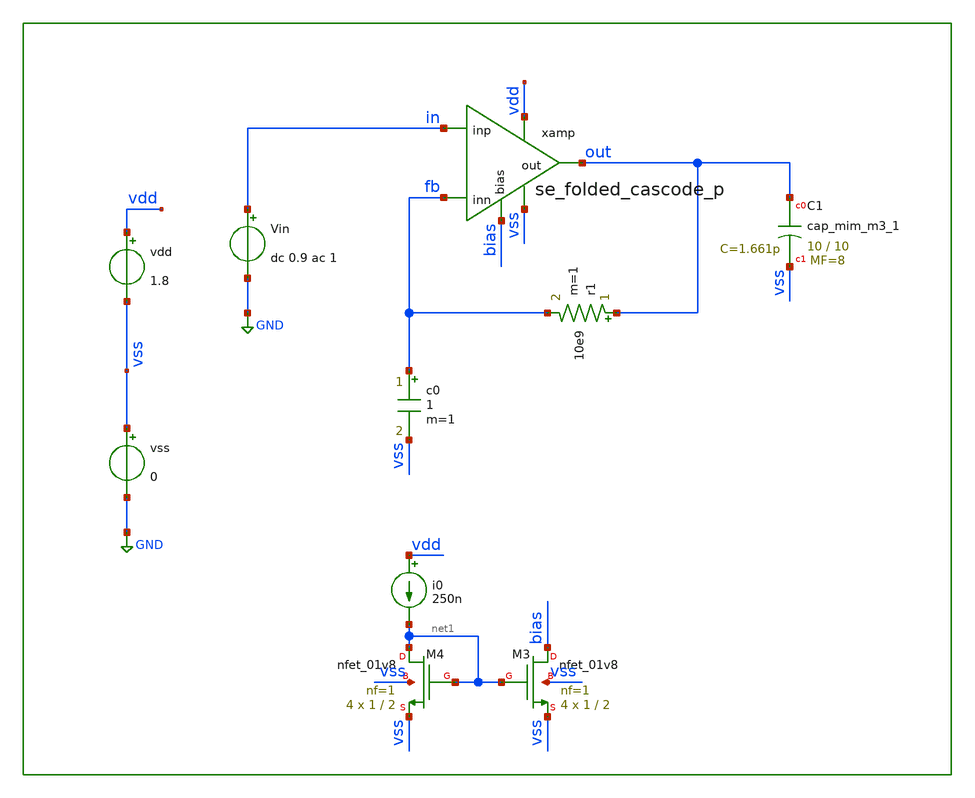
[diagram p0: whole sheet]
** sch_path: xschem/tb/opamp/ac_se_folded_ota_p.sch
**.subckt ac_se_folded_ota_p
vss vss GND 0
vdd vdd vss 1.8
Vin in GND dc 0.9 ac 1
c0 fb vss 1 m=1
r1 out fb 10e9 m=1
i0 vdd net1 250n
XM3 bias net1 vss vss sky130_fd_pr__nfet_01v8 L=2 W=1 nf=1 ad='int((nf+1)/2) * W/nf * 0.29' as='int((nf+2)/2) * W/nf * 0.29'
+ pd='2*int((nf+1)/2) * (W/nf + 0.29)' ps='2*int((nf+2)/2) * (W/nf + 0.29)' nrd='0.29 / W' nrs='0.29 / W'
+ sa=0 sb=0 sd=0 mult=4 m=4
XM4 net1 net1 vss vss sky130_fd_pr__nfet_01v8 L=2 W=1 nf=1 ad='int((nf+1)/2) * W/nf * 0.29' as='int((nf+2)/2) * W/nf * 0.29'
+ pd='2*int((nf+1)/2) * (W/nf + 0.29)' ps='2*int((nf+2)/2) * (W/nf + 0.29)' nrd='0.29 / W' nrs='0.29 / W'
+ sa=0 sb=0 sd=0 mult=4 m=4
xamp vdd out in fb vss bias se_folded_cascode_p
XC1 out vss sky130_fd_pr__cap_mim_m3_1 W=10 L=10 MF=8 m=8
**** begin user architecture code

* ac se_folded_cascode_p

.param MC_SWITCH=0
*.temp 85

*.include \$::DESIGN_PATH\/opamp/se_folded_cascode_p.pex.spice"

.control
save all
ac dec 10 1 100e6
let phase=180/3.14*cph(out)
let phase=180 + 180/3.14*cph(out)
meas ac ugbw when vdb(out)=0
meas ac pm find phase when vdb(out)=0
meas ac gain find vdb(out) at=1

*let mc_runs = 500
*let run = 1
*dowhile run <= mc_runs
*    save all
*    ac dec 10 1 100e6
*    let phase=180/3.14*cph(out)
*    let phase=180 + 180/3.14*cph(out)
*    meas ac ugbw when vdb(out)=0
*    meas ac pm find phase when vdb(out)=0
*    meas ac gain find vdb(out) at=100
*    print gain >> result_gain.txt
*    print pm >> result_pm.txt
*    print ugbw >> result_ugbw.txt
*    reset
*    let run = run + 1
*end


.endc


 .include $::SKYWATER_STDCELLS/cells/inv/sky130_fd_sc_hd__inv_1.spice

* FET CORNERS
.include $::SKYWATER_MODELS/corners/tt.spice
*.include $::SKYWATER_MODELS/corners/ff.spice
*.include $::SKYWATER_MODELS/corners/ss.spice
*.include $::SKYWATER_MODELS/corners/sf.spice
*.include $::SKYWATER_MODELS/corners/fs.spice

* TT + R + C
*.include $::SKYWATER_MODELS/corners/tt_rmax_cmax.spice
*.include $::SKYWATER_MODELS/corners/tt_rmin_cmin.spice
*.include $::SKYWATER_MODELS/corners/tt_rmax_cmin.spice
*.include $::SKYWATER_MODELS/corners/tt_rmin_cmax.spice

* FF + R + C
*.include $::SKYWATER_MODELS/corners/ff_rmax_cmax.spice
*.include $::SKYWATER_MODELS/corners/ff_rmin_cmin.spice
*.include $::SKYWATER_MODELS/corners/ff_rmax_cmin.spice
*.include $::SKYWATER_MODELS/corners/ff_rmin_cmax.spice


* SS + R + C
*.include $::SKYWATER_MODELS/corners/ss_rmax_cmax.spice
*.include $::SKYWATER_MODELS/corners/ss_rmin_cmin.spice
*.include $::SKYWATER_MODELS/corners/ss_rmax_cmin.spice
*.include $::SKYWATER_MODELS/corners/ss_rmin_cmax.spice

* SF + R + C
*.include $::SKYWATER_MODELS/corners/sf_rmax_cmax.spice
*.include $::SKYWATER_MODELS/corners/sf_rmin_cmin.spice
*.include $::SKYWATER_MODELS/corners/sf_rmax_cmin.spice
*.include $::SKYWATER_MODELS/corners/sf_rmin_cmax.spice

* FS + R + C
*.include $::SKYWATER_MODELS/corners/fs_rmax_cmax.spice
*.include $::SKYWATER_MODELS/corners/fs_rmin_cmin.spice
*.include $::SKYWATER_MODELS/corners/fs_rmax_cmin.spice
*.include $::SKYWATER_MODELS/corners/fs_rmin_cmax.spice

**** end user architecture code
**.ends

* expanding   symbol:  opamp/se_folded_cascode_p.sym # of pins=6
** sym_path: xschem/opamp/se_folded_cascode_p.sym
** sch_path: xschem/opamp/se_folded_cascode_p.sch
.subckt se_folded_cascode_p vdd out inp inn vss bias
*.ipin inn
*.ipin inp
*.opin out
*.iopin bias
*.iopin vdd
*.iopin vss
XM3 out1p inn diff vdd sky130_fd_pr__pfet_01v8_lvt L=1 W=4 nf=1 ad='int((nf+1)/2) * W/nf * 0.29' as='int((nf+2)/2) * W/nf * 0.29'
+ pd='2*int((nf+1)/2) * (W/nf + 0.29)' ps='2*int((nf+2)/2) * (W/nf + 0.29)' nrd='0.29 / W' nrs='0.29 / W'
+ sa=0 sb=0 sd=0 mult=8 m=8
XM2 out1n inp diff vdd sky130_fd_pr__pfet_01v8_lvt L=1 W=4 nf=1 ad='int((nf+1)/2) * W/nf * 0.29' as='int((nf+2)/2) * W/nf * 0.29'
+ pd='2*int((nf+1)/2) * (W/nf + 0.29)' ps='2*int((nf+2)/2) * (W/nf + 0.29)' nrd='0.29 / W' nrs='0.29 / W'
+ sa=0 sb=0 sd=0 mult=8 m=8
XM1 diff vbp1 vdd vdd sky130_fd_pr__pfet_01v8_lvt L=1 W=1 nf=1 ad='int((nf+1)/2) * W/nf * 0.29' as='int((nf+2)/2) * W/nf * 0.29'
+ pd='2*int((nf+1)/2) * (W/nf + 0.29)' ps='2*int((nf+2)/2) * (W/nf + 0.29)' nrd='0.29 / W' nrs='0.29 / W'
+ sa=0 sb=0 sd=0 mult=14 m=14
XM4 out1n vbn1 vss vss sky130_fd_pr__nfet_01v8_lvt L=1 W=1 nf=1 ad='int((nf+1)/2) * W/nf * 0.29' as='int((nf+2)/2) * W/nf * 0.29'
+ pd='2*int((nf+1)/2) * (W/nf + 0.29)' ps='2*int((nf+2)/2) * (W/nf + 0.29)' nrd='0.29 / W' nrs='0.29 / W'
+ sa=0 sb=0 sd=0 mult=16 m=16
XM5 out1p vbn1 vss vss sky130_fd_pr__nfet_01v8_lvt L=1 W=1 nf=1 ad='int((nf+1)/2) * W/nf * 0.29' as='int((nf+2)/2) * W/nf * 0.29'
+ pd='2*int((nf+1)/2) * (W/nf + 0.29)' ps='2*int((nf+2)/2) * (W/nf + 0.29)' nrd='0.29 / W' nrs='0.29 / W'
+ sa=0 sb=0 sd=0 mult=16 m=16
XM6 mirr vbn2 out1n vss sky130_fd_pr__nfet_01v8_lvt L=4 W=1 nf=1 ad='int((nf+1)/2) * W/nf * 0.29' as='int((nf+2)/2) * W/nf * 0.29'
+ pd='2*int((nf+1)/2) * (W/nf + 0.29)' ps='2*int((nf+2)/2) * (W/nf + 0.29)' nrd='0.29 / W' nrs='0.29 / W'
+ sa=0 sb=0 sd=0 mult=8 m=8
XM7 out vbn2 out1p vss sky130_fd_pr__nfet_01v8_lvt L=4 W=1 nf=1 ad='int((nf+1)/2) * W/nf * 0.29' as='int((nf+2)/2) * W/nf * 0.29'
+ pd='2*int((nf+1)/2) * (W/nf + 0.29)' ps='2*int((nf+2)/2) * (W/nf + 0.29)' nrd='0.29 / W' nrs='0.29 / W'
+ sa=0 sb=0 sd=0 mult=8 m=8
XM8 mirr bias nd10 vdd sky130_fd_pr__pfet_01v8_lvt L=4 W=2 nf=1 ad='int((nf+1)/2) * W/nf * 0.29' as='int((nf+2)/2) * W/nf * 0.29'
+ pd='2*int((nf+1)/2) * (W/nf + 0.29)' ps='2*int((nf+2)/2) * (W/nf + 0.29)' nrd='0.29 / W' nrs='0.29 / W'
+ sa=0 sb=0 sd=0 mult=8 m=8
XM9 out bias nd11 vdd sky130_fd_pr__pfet_01v8_lvt L=4 W=2 nf=1 ad='int((nf+1)/2) * W/nf * 0.29' as='int((nf+2)/2) * W/nf * 0.29'
+ pd='2*int((nf+1)/2) * (W/nf + 0.29)' ps='2*int((nf+2)/2) * (W/nf + 0.29)' nrd='0.29 / W' nrs='0.29 / W'
+ sa=0 sb=0 sd=0 mult=8 m=8
XM10 nd10 mirr vdd vdd sky130_fd_pr__pfet_01v8_lvt L=4 W=2 nf=1 ad='int((nf+1)/2) * W/nf * 0.29' as='int((nf+2)/2) * W/nf * 0.29'
+ pd='2*int((nf+1)/2) * (W/nf + 0.29)' ps='2*int((nf+2)/2) * (W/nf + 0.29)' nrd='0.29 / W' nrs='0.29 / W'
+ sa=0 sb=0 sd=0 mult=8 m=8
XM11 nd11 mirr vdd vdd sky130_fd_pr__pfet_01v8_lvt L=4 W=2 nf=1 ad='int((nf+1)/2) * W/nf * 0.29' as='int((nf+2)/2) * W/nf * 0.29'
+ pd='2*int((nf+1)/2) * (W/nf + 0.29)' ps='2*int((nf+2)/2) * (W/nf + 0.29)' nrd='0.29 / W' nrs='0.29 / W'
+ sa=0 sb=0 sd=0 mult=8 m=8
XMB1 bias bias vbp1 vdd sky130_fd_pr__pfet_01v8_lvt L=4 W=2 nf=1 ad='int((nf+1)/2) * W/nf * 0.29' as='int((nf+2)/2) * W/nf * 0.29'
+ pd='2*int((nf+1)/2) * (W/nf + 0.29)' ps='2*int((nf+2)/2) * (W/nf + 0.29)' nrd='0.29 / W' nrs='0.29 / W'
+ sa=0 sb=0 sd=0 mult=4 m=4
XMB2 vbp1 vbp1 vdd vdd sky130_fd_pr__pfet_01v8_lvt L=1 W=1 nf=1 ad='int((nf+1)/2) * W/nf * 0.29' as='int((nf+2)/2) * W/nf * 0.29'
+ pd='2*int((nf+1)/2) * (W/nf + 0.29)' ps='2*int((nf+2)/2) * (W/nf + 0.29)' nrd='0.29 / W' nrs='0.29 / W'
+ sa=0 sb=0 sd=0 mult=4 m=4
XMB3 vbn2 vbp1 vdd vdd sky130_fd_pr__pfet_01v8_lvt L=1 W=1 nf=1 ad='int((nf+1)/2) * W/nf * 0.29' as='int((nf+2)/2) * W/nf * 0.29'
+ pd='2*int((nf+1)/2) * (W/nf + 0.29)' ps='2*int((nf+2)/2) * (W/nf + 0.29)' nrd='0.29 / W' nrs='0.29 / W'
+ sa=0 sb=0 sd=0 mult=4 m=4
XMB4 vbn2 vbn2 vbn1 vss sky130_fd_pr__nfet_01v8_lvt L=4 W=1 nf=1 ad='int((nf+1)/2) * W/nf * 0.29' as='int((nf+2)/2) * W/nf * 0.29'
+ pd='2*int((nf+1)/2) * (W/nf + 0.29)' ps='2*int((nf+2)/2) * (W/nf + 0.29)' nrd='0.29 / W' nrs='0.29 / W'
+ sa=0 sb=0 sd=0 mult=4 m=4
XMB5 vbn1 vbn1 vss vss sky130_fd_pr__nfet_01v8_lvt L=1 W=1 nf=1 ad='int((nf+1)/2) * W/nf * 0.29' as='int((nf+2)/2) * W/nf * 0.29'
+ pd='2*int((nf+1)/2) * (W/nf + 0.29)' ps='2*int((nf+2)/2) * (W/nf + 0.29)' nrd='0.29 / W' nrs='0.29 / W'
+ sa=0 sb=0 sd=0 mult=4 m=4
XMDUM1[43] vdd vdd vdd vdd sky130_fd_pr__pfet_01v8_lvt L=4 W=2 nf=1 ad='int((nf+1)/2) * W/nf * 0.29'
+ as='int((nf+2)/2) * W/nf * 0.29' pd='2*int((nf+1)/2) * (W/nf + 0.29)' ps='2*int((nf+2)/2) * (W/nf + 0.29)'
+ nrd='0.29 / W' nrs='0.29 / W' sa=0 sb=0 sd=0 mult=1 m=1
XMDUM1[42] vdd vdd vdd vdd sky130_fd_pr__pfet_01v8_lvt L=4 W=2 nf=1 ad='int((nf+1)/2) * W/nf * 0.29'
+ as='int((nf+2)/2) * W/nf * 0.29' pd='2*int((nf+1)/2) * (W/nf + 0.29)' ps='2*int((nf+2)/2) * (W/nf + 0.29)'
+ nrd='0.29 / W' nrs='0.29 / W' sa=0 sb=0 sd=0 mult=1 m=1
XMDUM1[41] vdd vdd vdd vdd sky130_fd_pr__pfet_01v8_lvt L=4 W=2 nf=1 ad='int((nf+1)/2) * W/nf * 0.29'
+ as='int((nf+2)/2) * W/nf * 0.29' pd='2*int((nf+1)/2) * (W/nf + 0.29)' ps='2*int((nf+2)/2) * (W/nf + 0.29)'
+ nrd='0.29 / W' nrs='0.29 / W' sa=0 sb=0 sd=0 mult=1 m=1
XMDUM1[40] vdd vdd vdd vdd sky130_fd_pr__pfet_01v8_lvt L=4 W=2 nf=1 ad='int((nf+1)/2) * W/nf * 0.29'
+ as='int((nf+2)/2) * W/nf * 0.29' pd='2*int((nf+1)/2) * (W/nf + 0.29)' ps='2*int((nf+2)/2) * (W/nf + 0.29)'
+ nrd='0.29 / W' nrs='0.29 / W' sa=0 sb=0 sd=0 mult=1 m=1
XMDUM1[39] vdd vdd vdd vdd sky130_fd_pr__pfet_01v8_lvt L=4 W=2 nf=1 ad='int((nf+1)/2) * W/nf * 0.29'
+ as='int((nf+2)/2) * W/nf * 0.29' pd='2*int((nf+1)/2) * (W/nf + 0.29)' ps='2*int((nf+2)/2) * (W/nf + 0.29)'
+ nrd='0.29 / W' nrs='0.29 / W' sa=0 sb=0 sd=0 mult=1 m=1
XMDUM1[38] vdd vdd vdd vdd sky130_fd_pr__pfet_01v8_lvt L=4 W=2 nf=1 ad='int((nf+1)/2) * W/nf * 0.29'
+ as='int((nf+2)/2) * W/nf * 0.29' pd='2*int((nf+1)/2) * (W/nf + 0.29)' ps='2*int((nf+2)/2) * (W/nf + 0.29)'
+ nrd='0.29 / W' nrs='0.29 / W' sa=0 sb=0 sd=0 mult=1 m=1
XMDUM1[37] vdd vdd vdd vdd sky130_fd_pr__pfet_01v8_lvt L=4 W=2 nf=1 ad='int((nf+1)/2) * W/nf * 0.29'
+ as='int((nf+2)/2) * W/nf * 0.29' pd='2*int((nf+1)/2) * (W/nf + 0.29)' ps='2*int((nf+2)/2) * (W/nf + 0.29)'
+ nrd='0.29 / W' nrs='0.29 / W' sa=0 sb=0 sd=0 mult=1 m=1
XMDUM1[36] vdd vdd vdd vdd sky130_fd_pr__pfet_01v8_lvt L=4 W=2 nf=1 ad='int((nf+1)/2) * W/nf * 0.29'
+ as='int((nf+2)/2) * W/nf * 0.29' pd='2*int((nf+1)/2) * (W/nf + 0.29)' ps='2*int((nf+2)/2) * (W/nf + 0.29)'
+ nrd='0.29 / W' nrs='0.29 / W' sa=0 sb=0 sd=0 mult=1 m=1
XMDUM1[35] vdd vdd vdd vdd sky130_fd_pr__pfet_01v8_lvt L=4 W=2 nf=1 ad='int((nf+1)/2) * W/nf * 0.29'
+ as='int((nf+2)/2) * W/nf * 0.29' pd='2*int((nf+1)/2) * (W/nf + 0.29)' ps='2*int((nf+2)/2) * (W/nf + 0.29)'
+ nrd='0.29 / W' nrs='0.29 / W' sa=0 sb=0 sd=0 mult=1 m=1
XMDUM1[34] vdd vdd vdd vdd sky130_fd_pr__pfet_01v8_lvt L=4 W=2 nf=1 ad='int((nf+1)/2) * W/nf * 0.29'
+ as='int((nf+2)/2) * W/nf * 0.29' pd='2*int((nf+1)/2) * (W/nf + 0.29)' ps='2*int((nf+2)/2) * (W/nf + 0.29)'
+ nrd='0.29 / W' nrs='0.29 / W' sa=0 sb=0 sd=0 mult=1 m=1
XMDUM1[33] vdd vdd vdd vdd sky130_fd_pr__pfet_01v8_lvt L=4 W=2 nf=1 ad='int((nf+1)/2) * W/nf * 0.29'
+ as='int((nf+2)/2) * W/nf * 0.29' pd='2*int((nf+1)/2) * (W/nf + 0.29)' ps='2*int((nf+2)/2) * (W/nf + 0.29)'
+ nrd='0.29 / W' nrs='0.29 / W' sa=0 sb=0 sd=0 mult=1 m=1
XMDUM1[32] vdd vdd vdd vdd sky130_fd_pr__pfet_01v8_lvt L=4 W=2 nf=1 ad='int((nf+1)/2) * W/nf * 0.29'
+ as='int((nf+2)/2) * W/nf * 0.29' pd='2*int((nf+1)/2) * (W/nf + 0.29)' ps='2*int((nf+2)/2) * (W/nf + 0.29)'
+ nrd='0.29 / W' nrs='0.29 / W' sa=0 sb=0 sd=0 mult=1 m=1
XMDUM1[31] vdd vdd vdd vdd sky130_fd_pr__pfet_01v8_lvt L=4 W=2 nf=1 ad='int((nf+1)/2) * W/nf * 0.29'
+ as='int((nf+2)/2) * W/nf * 0.29' pd='2*int((nf+1)/2) * (W/nf + 0.29)' ps='2*int((nf+2)/2) * (W/nf + 0.29)'
+ nrd='0.29 / W' nrs='0.29 / W' sa=0 sb=0 sd=0 mult=1 m=1
XMDUM1[30] vdd vdd vdd vdd sky130_fd_pr__pfet_01v8_lvt L=4 W=2 nf=1 ad='int((nf+1)/2) * W/nf * 0.29'
+ as='int((nf+2)/2) * W/nf * 0.29' pd='2*int((nf+1)/2) * (W/nf + 0.29)' ps='2*int((nf+2)/2) * (W/nf + 0.29)'
+ nrd='0.29 / W' nrs='0.29 / W' sa=0 sb=0 sd=0 mult=1 m=1
XMDUM1[29] vdd vdd vdd vdd sky130_fd_pr__pfet_01v8_lvt L=4 W=2 nf=1 ad='int((nf+1)/2) * W/nf * 0.29'
+ as='int((nf+2)/2) * W/nf * 0.29' pd='2*int((nf+1)/2) * (W/nf + 0.29)' ps='2*int((nf+2)/2) * (W/nf + 0.29)'
+ nrd='0.29 / W' nrs='0.29 / W' sa=0 sb=0 sd=0 mult=1 m=1
XMDUM1[28] vdd vdd vdd vdd sky130_fd_pr__pfet_01v8_lvt L=4 W=2 nf=1 ad='int((nf+1)/2) * W/nf * 0.29'
+ as='int((nf+2)/2) * W/nf * 0.29' pd='2*int((nf+1)/2) * (W/nf + 0.29)' ps='2*int((nf+2)/2) * (W/nf + 0.29)'
+ nrd='0.29 / W' nrs='0.29 / W' sa=0 sb=0 sd=0 mult=1 m=1
XMDUM1[27] vdd vdd vdd vdd sky130_fd_pr__pfet_01v8_lvt L=4 W=2 nf=1 ad='int((nf+1)/2) * W/nf * 0.29'
+ as='int((nf+2)/2) * W/nf * 0.29' pd='2*int((nf+1)/2) * (W/nf + 0.29)' ps='2*int((nf+2)/2) * (W/nf + 0.29)'
+ nrd='0.29 / W' nrs='0.29 / W' sa=0 sb=0 sd=0 mult=1 m=1
XMDUM1[26] vdd vdd vdd vdd sky130_fd_pr__pfet_01v8_lvt L=4 W=2 nf=1 ad='int((nf+1)/2) * W/nf * 0.29'
+ as='int((nf+2)/2) * W/nf * 0.29' pd='2*int((nf+1)/2) * (W/nf + 0.29)' ps='2*int((nf+2)/2) * (W/nf + 0.29)'
+ nrd='0.29 / W' nrs='0.29 / W' sa=0 sb=0 sd=0 mult=1 m=1
XMDUM1[25] vdd vdd vdd vdd sky130_fd_pr__pfet_01v8_lvt L=4 W=2 nf=1 ad='int((nf+1)/2) * W/nf * 0.29'
+ as='int((nf+2)/2) * W/nf * 0.29' pd='2*int((nf+1)/2) * (W/nf + 0.29)' ps='2*int((nf+2)/2) * (W/nf + 0.29)'
+ nrd='0.29 / W' nrs='0.29 / W' sa=0 sb=0 sd=0 mult=1 m=1
XMDUM1[24] vdd vdd vdd vdd sky130_fd_pr__pfet_01v8_lvt L=4 W=2 nf=1 ad='int((nf+1)/2) * W/nf * 0.29'
+ as='int((nf+2)/2) * W/nf * 0.29' pd='2*int((nf+1)/2) * (W/nf + 0.29)' ps='2*int((nf+2)/2) * (W/nf + 0.29)'
+ nrd='0.29 / W' nrs='0.29 / W' sa=0 sb=0 sd=0 mult=1 m=1
XMDUM1[23] vdd vdd vdd vdd sky130_fd_pr__pfet_01v8_lvt L=4 W=2 nf=1 ad='int((nf+1)/2) * W/nf * 0.29'
+ as='int((nf+2)/2) * W/nf * 0.29' pd='2*int((nf+1)/2) * (W/nf + 0.29)' ps='2*int((nf+2)/2) * (W/nf + 0.29)'
+ nrd='0.29 / W' nrs='0.29 / W' sa=0 sb=0 sd=0 mult=1 m=1
XMDUM1[22] vdd vdd vdd vdd sky130_fd_pr__pfet_01v8_lvt L=4 W=2 nf=1 ad='int((nf+1)/2) * W/nf * 0.29'
+ as='int((nf+2)/2) * W/nf * 0.29' pd='2*int((nf+1)/2) * (W/nf + 0.29)' ps='2*int((nf+2)/2) * (W/nf + 0.29)'
+ nrd='0.29 / W' nrs='0.29 / W' sa=0 sb=0 sd=0 mult=1 m=1
XMDUM1[21] vdd vdd vdd vdd sky130_fd_pr__pfet_01v8_lvt L=4 W=2 nf=1 ad='int((nf+1)/2) * W/nf * 0.29'
+ as='int((nf+2)/2) * W/nf * 0.29' pd='2*int((nf+1)/2) * (W/nf + 0.29)' ps='2*int((nf+2)/2) * (W/nf + 0.29)'
+ nrd='0.29 / W' nrs='0.29 / W' sa=0 sb=0 sd=0 mult=1 m=1
XMDUM1[20] vdd vdd vdd vdd sky130_fd_pr__pfet_01v8_lvt L=4 W=2 nf=1 ad='int((nf+1)/2) * W/nf * 0.29'
+ as='int((nf+2)/2) * W/nf * 0.29' pd='2*int((nf+1)/2) * (W/nf + 0.29)' ps='2*int((nf+2)/2) * (W/nf + 0.29)'
+ nrd='0.29 / W' nrs='0.29 / W' sa=0 sb=0 sd=0 mult=1 m=1
XMDUM1[19] vdd vdd vdd vdd sky130_fd_pr__pfet_01v8_lvt L=4 W=2 nf=1 ad='int((nf+1)/2) * W/nf * 0.29'
+ as='int((nf+2)/2) * W/nf * 0.29' pd='2*int((nf+1)/2) * (W/nf + 0.29)' ps='2*int((nf+2)/2) * (W/nf + 0.29)'
+ nrd='0.29 / W' nrs='0.29 / W' sa=0 sb=0 sd=0 mult=1 m=1
XMDUM1[18] vdd vdd vdd vdd sky130_fd_pr__pfet_01v8_lvt L=4 W=2 nf=1 ad='int((nf+1)/2) * W/nf * 0.29'
+ as='int((nf+2)/2) * W/nf * 0.29' pd='2*int((nf+1)/2) * (W/nf + 0.29)' ps='2*int((nf+2)/2) * (W/nf + 0.29)'
+ nrd='0.29 / W' nrs='0.29 / W' sa=0 sb=0 sd=0 mult=1 m=1
XMDUM1[17] vdd vdd vdd vdd sky130_fd_pr__pfet_01v8_lvt L=4 W=2 nf=1 ad='int((nf+1)/2) * W/nf * 0.29'
+ as='int((nf+2)/2) * W/nf * 0.29' pd='2*int((nf+1)/2) * (W/nf + 0.29)' ps='2*int((nf+2)/2) * (W/nf + 0.29)'
+ nrd='0.29 / W' nrs='0.29 / W' sa=0 sb=0 sd=0 mult=1 m=1
XMDUM1[16] vdd vdd vdd vdd sky130_fd_pr__pfet_01v8_lvt L=4 W=2 nf=1 ad='int((nf+1)/2) * W/nf * 0.29'
+ as='int((nf+2)/2) * W/nf * 0.29' pd='2*int((nf+1)/2) * (W/nf + 0.29)' ps='2*int((nf+2)/2) * (W/nf + 0.29)'
+ nrd='0.29 / W' nrs='0.29 / W' sa=0 sb=0 sd=0 mult=1 m=1
XMDUM1[15] vdd vdd vdd vdd sky130_fd_pr__pfet_01v8_lvt L=4 W=2 nf=1 ad='int((nf+1)/2) * W/nf * 0.29'
+ as='int((nf+2)/2) * W/nf * 0.29' pd='2*int((nf+1)/2) * (W/nf + 0.29)' ps='2*int((nf+2)/2) * (W/nf + 0.29)'
+ nrd='0.29 / W' nrs='0.29 / W' sa=0 sb=0 sd=0 mult=1 m=1
XMDUM1[14] vdd vdd vdd vdd sky130_fd_pr__pfet_01v8_lvt L=4 W=2 nf=1 ad='int((nf+1)/2) * W/nf * 0.29'
+ as='int((nf+2)/2) * W/nf * 0.29' pd='2*int((nf+1)/2) * (W/nf + 0.29)' ps='2*int((nf+2)/2) * (W/nf + 0.29)'
+ nrd='0.29 / W' nrs='0.29 / W' sa=0 sb=0 sd=0 mult=1 m=1
XMDUM1[13] vdd vdd vdd vdd sky130_fd_pr__pfet_01v8_lvt L=4 W=2 nf=1 ad='int((nf+1)/2) * W/nf * 0.29'
+ as='int((nf+2)/2) * W/nf * 0.29' pd='2*int((nf+1)/2) * (W/nf + 0.29)' ps='2*int((nf+2)/2) * (W/nf + 0.29)'
+ nrd='0.29 / W' nrs='0.29 / W' sa=0 sb=0 sd=0 mult=1 m=1
XMDUM1[12] vdd vdd vdd vdd sky130_fd_pr__pfet_01v8_lvt L=4 W=2 nf=1 ad='int((nf+1)/2) * W/nf * 0.29'
+ as='int((nf+2)/2) * W/nf * 0.29' pd='2*int((nf+1)/2) * (W/nf + 0.29)' ps='2*int((nf+2)/2) * (W/nf + 0.29)'
+ nrd='0.29 / W' nrs='0.29 / W' sa=0 sb=0 sd=0 mult=1 m=1
XMDUM1[11] vdd vdd vdd vdd sky130_fd_pr__pfet_01v8_lvt L=4 W=2 nf=1 ad='int((nf+1)/2) * W/nf * 0.29'
+ as='int((nf+2)/2) * W/nf * 0.29' pd='2*int((nf+1)/2) * (W/nf + 0.29)' ps='2*int((nf+2)/2) * (W/nf + 0.29)'
+ nrd='0.29 / W' nrs='0.29 / W' sa=0 sb=0 sd=0 mult=1 m=1
XMDUM1[10] vdd vdd vdd vdd sky130_fd_pr__pfet_01v8_lvt L=4 W=2 nf=1 ad='int((nf+1)/2) * W/nf * 0.29'
+ as='int((nf+2)/2) * W/nf * 0.29' pd='2*int((nf+1)/2) * (W/nf + 0.29)' ps='2*int((nf+2)/2) * (W/nf + 0.29)'
+ nrd='0.29 / W' nrs='0.29 / W' sa=0 sb=0 sd=0 mult=1 m=1
XMDUM1[9] vdd vdd vdd vdd sky130_fd_pr__pfet_01v8_lvt L=4 W=2 nf=1 ad='int((nf+1)/2) * W/nf * 0.29' as='int((nf+2)/2) * W/nf * 0.29'
+ pd='2*int((nf+1)/2) * (W/nf + 0.29)' ps='2*int((nf+2)/2) * (W/nf + 0.29)' nrd='0.29 / W' nrs='0.29 / W'
+ sa=0 sb=0 sd=0 mult=1 m=1
XMDUM1[8] vdd vdd vdd vdd sky130_fd_pr__pfet_01v8_lvt L=4 W=2 nf=1 ad='int((nf+1)/2) * W/nf * 0.29' as='int((nf+2)/2) * W/nf * 0.29'
+ pd='2*int((nf+1)/2) * (W/nf + 0.29)' ps='2*int((nf+2)/2) * (W/nf + 0.29)' nrd='0.29 / W' nrs='0.29 / W'
+ sa=0 sb=0 sd=0 mult=1 m=1
XMDUM1[7] vdd vdd vdd vdd sky130_fd_pr__pfet_01v8_lvt L=4 W=2 nf=1 ad='int((nf+1)/2) * W/nf * 0.29' as='int((nf+2)/2) * W/nf * 0.29'
+ pd='2*int((nf+1)/2) * (W/nf + 0.29)' ps='2*int((nf+2)/2) * (W/nf + 0.29)' nrd='0.29 / W' nrs='0.29 / W'
+ sa=0 sb=0 sd=0 mult=1 m=1
XMDUM1[6] vdd vdd vdd vdd sky130_fd_pr__pfet_01v8_lvt L=4 W=2 nf=1 ad='int((nf+1)/2) * W/nf * 0.29' as='int((nf+2)/2) * W/nf * 0.29'
+ pd='2*int((nf+1)/2) * (W/nf + 0.29)' ps='2*int((nf+2)/2) * (W/nf + 0.29)' nrd='0.29 / W' nrs='0.29 / W'
+ sa=0 sb=0 sd=0 mult=1 m=1
XMDUM1[5] vdd vdd vdd vdd sky130_fd_pr__pfet_01v8_lvt L=4 W=2 nf=1 ad='int((nf+1)/2) * W/nf * 0.29' as='int((nf+2)/2) * W/nf * 0.29'
+ pd='2*int((nf+1)/2) * (W/nf + 0.29)' ps='2*int((nf+2)/2) * (W/nf + 0.29)' nrd='0.29 / W' nrs='0.29 / W'
+ sa=0 sb=0 sd=0 mult=1 m=1
XMDUM1[4] vdd vdd vdd vdd sky130_fd_pr__pfet_01v8_lvt L=4 W=2 nf=1 ad='int((nf+1)/2) * W/nf * 0.29' as='int((nf+2)/2) * W/nf * 0.29'
+ pd='2*int((nf+1)/2) * (W/nf + 0.29)' ps='2*int((nf+2)/2) * (W/nf + 0.29)' nrd='0.29 / W' nrs='0.29 / W'
+ sa=0 sb=0 sd=0 mult=1 m=1
XMDUM1[3] vdd vdd vdd vdd sky130_fd_pr__pfet_01v8_lvt L=4 W=2 nf=1 ad='int((nf+1)/2) * W/nf * 0.29' as='int((nf+2)/2) * W/nf * 0.29'
+ pd='2*int((nf+1)/2) * (W/nf + 0.29)' ps='2*int((nf+2)/2) * (W/nf + 0.29)' nrd='0.29 / W' nrs='0.29 / W'
+ sa=0 sb=0 sd=0 mult=1 m=1
XMDUM1[2] vdd vdd vdd vdd sky130_fd_pr__pfet_01v8_lvt L=4 W=2 nf=1 ad='int((nf+1)/2) * W/nf * 0.29' as='int((nf+2)/2) * W/nf * 0.29'
+ pd='2*int((nf+1)/2) * (W/nf + 0.29)' ps='2*int((nf+2)/2) * (W/nf + 0.29)' nrd='0.29 / W' nrs='0.29 / W'
+ sa=0 sb=0 sd=0 mult=1 m=1
XMDUM1[1] vdd vdd vdd vdd sky130_fd_pr__pfet_01v8_lvt L=4 W=2 nf=1 ad='int((nf+1)/2) * W/nf * 0.29' as='int((nf+2)/2) * W/nf * 0.29'
+ pd='2*int((nf+1)/2) * (W/nf + 0.29)' ps='2*int((nf+2)/2) * (W/nf + 0.29)' nrd='0.29 / W' nrs='0.29 / W'
+ sa=0 sb=0 sd=0 mult=1 m=1
XMDUM1[0] vdd vdd vdd vdd sky130_fd_pr__pfet_01v8_lvt L=4 W=2 nf=1 ad='int((nf+1)/2) * W/nf * 0.29' as='int((nf+2)/2) * W/nf * 0.29'
+ pd='2*int((nf+1)/2) * (W/nf + 0.29)' ps='2*int((nf+2)/2) * (W/nf + 0.29)' nrd='0.29 / W' nrs='0.29 / W'
+ sa=0 sb=0 sd=0 mult=1 m=1
XMDUM2[3] mirr mirr mirr vdd sky130_fd_pr__pfet_01v8_lvt L=4 W=2 nf=1 ad='int((nf+1)/2) * W/nf * 0.29'
+ as='int((nf+2)/2) * W/nf * 0.29' pd='2*int((nf+1)/2) * (W/nf + 0.29)' ps='2*int((nf+2)/2) * (W/nf + 0.29)'
+ nrd='0.29 / W' nrs='0.29 / W' sa=0 sb=0 sd=0 mult=1 m=1
XMDUM2[2] mirr mirr mirr vdd sky130_fd_pr__pfet_01v8_lvt L=4 W=2 nf=1 ad='int((nf+1)/2) * W/nf * 0.29'
+ as='int((nf+2)/2) * W/nf * 0.29' pd='2*int((nf+1)/2) * (W/nf + 0.29)' ps='2*int((nf+2)/2) * (W/nf + 0.29)'
+ nrd='0.29 / W' nrs='0.29 / W' sa=0 sb=0 sd=0 mult=1 m=1
XMDUM2[1] mirr mirr mirr vdd sky130_fd_pr__pfet_01v8_lvt L=4 W=2 nf=1 ad='int((nf+1)/2) * W/nf * 0.29'
+ as='int((nf+2)/2) * W/nf * 0.29' pd='2*int((nf+1)/2) * (W/nf + 0.29)' ps='2*int((nf+2)/2) * (W/nf + 0.29)'
+ nrd='0.29 / W' nrs='0.29 / W' sa=0 sb=0 sd=0 mult=1 m=1
XMDUM2[0] mirr mirr mirr vdd sky130_fd_pr__pfet_01v8_lvt L=4 W=2 nf=1 ad='int((nf+1)/2) * W/nf * 0.29'
+ as='int((nf+2)/2) * W/nf * 0.29' pd='2*int((nf+1)/2) * (W/nf + 0.29)' ps='2*int((nf+2)/2) * (W/nf + 0.29)'
+ nrd='0.29 / W' nrs='0.29 / W' sa=0 sb=0 sd=0 mult=1 m=1
XMDUM3[3] bias bias bias vdd sky130_fd_pr__pfet_01v8_lvt L=4 W=2 nf=1 ad='int((nf+1)/2) * W/nf * 0.29'
+ as='int((nf+2)/2) * W/nf * 0.29' pd='2*int((nf+1)/2) * (W/nf + 0.29)' ps='2*int((nf+2)/2) * (W/nf + 0.29)'
+ nrd='0.29 / W' nrs='0.29 / W' sa=0 sb=0 sd=0 mult=1 m=1
XMDUM3[2] bias bias bias vdd sky130_fd_pr__pfet_01v8_lvt L=4 W=2 nf=1 ad='int((nf+1)/2) * W/nf * 0.29'
+ as='int((nf+2)/2) * W/nf * 0.29' pd='2*int((nf+1)/2) * (W/nf + 0.29)' ps='2*int((nf+2)/2) * (W/nf + 0.29)'
+ nrd='0.29 / W' nrs='0.29 / W' sa=0 sb=0 sd=0 mult=1 m=1
XMDUM3[1] bias bias bias vdd sky130_fd_pr__pfet_01v8_lvt L=4 W=2 nf=1 ad='int((nf+1)/2) * W/nf * 0.29'
+ as='int((nf+2)/2) * W/nf * 0.29' pd='2*int((nf+1)/2) * (W/nf + 0.29)' ps='2*int((nf+2)/2) * (W/nf + 0.29)'
+ nrd='0.29 / W' nrs='0.29 / W' sa=0 sb=0 sd=0 mult=1 m=1
XMDUM3[0] bias bias bias vdd sky130_fd_pr__pfet_01v8_lvt L=4 W=2 nf=1 ad='int((nf+1)/2) * W/nf * 0.29'
+ as='int((nf+2)/2) * W/nf * 0.29' pd='2*int((nf+1)/2) * (W/nf + 0.29)' ps='2*int((nf+2)/2) * (W/nf + 0.29)'
+ nrd='0.29 / W' nrs='0.29 / W' sa=0 sb=0 sd=0 mult=1 m=1
XMDUM4[23] vss vss vss vss sky130_fd_pr__nfet_01v8_lvt L=4 W=1 nf=1 ad='int((nf+1)/2) * W/nf * 0.29'
+ as='int((nf+2)/2) * W/nf * 0.29' pd='2*int((nf+1)/2) * (W/nf + 0.29)' ps='2*int((nf+2)/2) * (W/nf + 0.29)'
+ nrd='0.29 / W' nrs='0.29 / W' sa=0 sb=0 sd=0 mult=1 m=1
XMDUM4[22] vss vss vss vss sky130_fd_pr__nfet_01v8_lvt L=4 W=1 nf=1 ad='int((nf+1)/2) * W/nf * 0.29'
+ as='int((nf+2)/2) * W/nf * 0.29' pd='2*int((nf+1)/2) * (W/nf + 0.29)' ps='2*int((nf+2)/2) * (W/nf + 0.29)'
+ nrd='0.29 / W' nrs='0.29 / W' sa=0 sb=0 sd=0 mult=1 m=1
XMDUM4[21] vss vss vss vss sky130_fd_pr__nfet_01v8_lvt L=4 W=1 nf=1 ad='int((nf+1)/2) * W/nf * 0.29'
+ as='int((nf+2)/2) * W/nf * 0.29' pd='2*int((nf+1)/2) * (W/nf + 0.29)' ps='2*int((nf+2)/2) * (W/nf + 0.29)'
+ nrd='0.29 / W' nrs='0.29 / W' sa=0 sb=0 sd=0 mult=1 m=1
XMDUM4[20] vss vss vss vss sky130_fd_pr__nfet_01v8_lvt L=4 W=1 nf=1 ad='int((nf+1)/2) * W/nf * 0.29'
+ as='int((nf+2)/2) * W/nf * 0.29' pd='2*int((nf+1)/2) * (W/nf + 0.29)' ps='2*int((nf+2)/2) * (W/nf + 0.29)'
+ nrd='0.29 / W' nrs='0.29 / W' sa=0 sb=0 sd=0 mult=1 m=1
XMDUM4[19] vss vss vss vss sky130_fd_pr__nfet_01v8_lvt L=4 W=1 nf=1 ad='int((nf+1)/2) * W/nf * 0.29'
+ as='int((nf+2)/2) * W/nf * 0.29' pd='2*int((nf+1)/2) * (W/nf + 0.29)' ps='2*int((nf+2)/2) * (W/nf + 0.29)'
+ nrd='0.29 / W' nrs='0.29 / W' sa=0 sb=0 sd=0 mult=1 m=1
XMDUM4[18] vss vss vss vss sky130_fd_pr__nfet_01v8_lvt L=4 W=1 nf=1 ad='int((nf+1)/2) * W/nf * 0.29'
+ as='int((nf+2)/2) * W/nf * 0.29' pd='2*int((nf+1)/2) * (W/nf + 0.29)' ps='2*int((nf+2)/2) * (W/nf + 0.29)'
+ nrd='0.29 / W' nrs='0.29 / W' sa=0 sb=0 sd=0 mult=1 m=1
XMDUM4[17] vss vss vss vss sky130_fd_pr__nfet_01v8_lvt L=4 W=1 nf=1 ad='int((nf+1)/2) * W/nf * 0.29'
+ as='int((nf+2)/2) * W/nf * 0.29' pd='2*int((nf+1)/2) * (W/nf + 0.29)' ps='2*int((nf+2)/2) * (W/nf + 0.29)'
+ nrd='0.29 / W' nrs='0.29 / W' sa=0 sb=0 sd=0 mult=1 m=1
XMDUM4[16] vss vss vss vss sky130_fd_pr__nfet_01v8_lvt L=4 W=1 nf=1 ad='int((nf+1)/2) * W/nf * 0.29'
+ as='int((nf+2)/2) * W/nf * 0.29' pd='2*int((nf+1)/2) * (W/nf + 0.29)' ps='2*int((nf+2)/2) * (W/nf + 0.29)'
+ nrd='0.29 / W' nrs='0.29 / W' sa=0 sb=0 sd=0 mult=1 m=1
XMDUM4[15] vss vss vss vss sky130_fd_pr__nfet_01v8_lvt L=4 W=1 nf=1 ad='int((nf+1)/2) * W/nf * 0.29'
+ as='int((nf+2)/2) * W/nf * 0.29' pd='2*int((nf+1)/2) * (W/nf + 0.29)' ps='2*int((nf+2)/2) * (W/nf + 0.29)'
+ nrd='0.29 / W' nrs='0.29 / W' sa=0 sb=0 sd=0 mult=1 m=1
XMDUM4[14] vss vss vss vss sky130_fd_pr__nfet_01v8_lvt L=4 W=1 nf=1 ad='int((nf+1)/2) * W/nf * 0.29'
+ as='int((nf+2)/2) * W/nf * 0.29' pd='2*int((nf+1)/2) * (W/nf + 0.29)' ps='2*int((nf+2)/2) * (W/nf + 0.29)'
+ nrd='0.29 / W' nrs='0.29 / W' sa=0 sb=0 sd=0 mult=1 m=1
XMDUM4[13] vss vss vss vss sky130_fd_pr__nfet_01v8_lvt L=4 W=1 nf=1 ad='int((nf+1)/2) * W/nf * 0.29'
+ as='int((nf+2)/2) * W/nf * 0.29' pd='2*int((nf+1)/2) * (W/nf + 0.29)' ps='2*int((nf+2)/2) * (W/nf + 0.29)'
+ nrd='0.29 / W' nrs='0.29 / W' sa=0 sb=0 sd=0 mult=1 m=1
XMDUM4[12] vss vss vss vss sky130_fd_pr__nfet_01v8_lvt L=4 W=1 nf=1 ad='int((nf+1)/2) * W/nf * 0.29'
+ as='int((nf+2)/2) * W/nf * 0.29' pd='2*int((nf+1)/2) * (W/nf + 0.29)' ps='2*int((nf+2)/2) * (W/nf + 0.29)'
+ nrd='0.29 / W' nrs='0.29 / W' sa=0 sb=0 sd=0 mult=1 m=1
XMDUM4[11] vss vss vss vss sky130_fd_pr__nfet_01v8_lvt L=4 W=1 nf=1 ad='int((nf+1)/2) * W/nf * 0.29'
+ as='int((nf+2)/2) * W/nf * 0.29' pd='2*int((nf+1)/2) * (W/nf + 0.29)' ps='2*int((nf+2)/2) * (W/nf + 0.29)'
+ nrd='0.29 / W' nrs='0.29 / W' sa=0 sb=0 sd=0 mult=1 m=1
XMDUM4[10] vss vss vss vss sky130_fd_pr__nfet_01v8_lvt L=4 W=1 nf=1 ad='int((nf+1)/2) * W/nf * 0.29'
+ as='int((nf+2)/2) * W/nf * 0.29' pd='2*int((nf+1)/2) * (W/nf + 0.29)' ps='2*int((nf+2)/2) * (W/nf + 0.29)'
+ nrd='0.29 / W' nrs='0.29 / W' sa=0 sb=0 sd=0 mult=1 m=1
XMDUM4[9] vss vss vss vss sky130_fd_pr__nfet_01v8_lvt L=4 W=1 nf=1 ad='int((nf+1)/2) * W/nf * 0.29' as='int((nf+2)/2) * W/nf * 0.29'
+ pd='2*int((nf+1)/2) * (W/nf + 0.29)' ps='2*int((nf+2)/2) * (W/nf + 0.29)' nrd='0.29 / W' nrs='0.29 / W'
+ sa=0 sb=0 sd=0 mult=1 m=1
XMDUM4[8] vss vss vss vss sky130_fd_pr__nfet_01v8_lvt L=4 W=1 nf=1 ad='int((nf+1)/2) * W/nf * 0.29' as='int((nf+2)/2) * W/nf * 0.29'
+ pd='2*int((nf+1)/2) * (W/nf + 0.29)' ps='2*int((nf+2)/2) * (W/nf + 0.29)' nrd='0.29 / W' nrs='0.29 / W'
+ sa=0 sb=0 sd=0 mult=1 m=1
XMDUM4[7] vss vss vss vss sky130_fd_pr__nfet_01v8_lvt L=4 W=1 nf=1 ad='int((nf+1)/2) * W/nf * 0.29' as='int((nf+2)/2) * W/nf * 0.29'
+ pd='2*int((nf+1)/2) * (W/nf + 0.29)' ps='2*int((nf+2)/2) * (W/nf + 0.29)' nrd='0.29 / W' nrs='0.29 / W'
+ sa=0 sb=0 sd=0 mult=1 m=1
XMDUM4[6] vss vss vss vss sky130_fd_pr__nfet_01v8_lvt L=4 W=1 nf=1 ad='int((nf+1)/2) * W/nf * 0.29' as='int((nf+2)/2) * W/nf * 0.29'
+ pd='2*int((nf+1)/2) * (W/nf + 0.29)' ps='2*int((nf+2)/2) * (W/nf + 0.29)' nrd='0.29 / W' nrs='0.29 / W'
+ sa=0 sb=0 sd=0 mult=1 m=1
XMDUM4[5] vss vss vss vss sky130_fd_pr__nfet_01v8_lvt L=4 W=1 nf=1 ad='int((nf+1)/2) * W/nf * 0.29' as='int((nf+2)/2) * W/nf * 0.29'
+ pd='2*int((nf+1)/2) * (W/nf + 0.29)' ps='2*int((nf+2)/2) * (W/nf + 0.29)' nrd='0.29 / W' nrs='0.29 / W'
+ sa=0 sb=0 sd=0 mult=1 m=1
XMDUM4[4] vss vss vss vss sky130_fd_pr__nfet_01v8_lvt L=4 W=1 nf=1 ad='int((nf+1)/2) * W/nf * 0.29' as='int((nf+2)/2) * W/nf * 0.29'
+ pd='2*int((nf+1)/2) * (W/nf + 0.29)' ps='2*int((nf+2)/2) * (W/nf + 0.29)' nrd='0.29 / W' nrs='0.29 / W'
+ sa=0 sb=0 sd=0 mult=1 m=1
XMDUM4[3] vss vss vss vss sky130_fd_pr__nfet_01v8_lvt L=4 W=1 nf=1 ad='int((nf+1)/2) * W/nf * 0.29' as='int((nf+2)/2) * W/nf * 0.29'
+ pd='2*int((nf+1)/2) * (W/nf + 0.29)' ps='2*int((nf+2)/2) * (W/nf + 0.29)' nrd='0.29 / W' nrs='0.29 / W'
+ sa=0 sb=0 sd=0 mult=1 m=1
XMDUM4[2] vss vss vss vss sky130_fd_pr__nfet_01v8_lvt L=4 W=1 nf=1 ad='int((nf+1)/2) * W/nf * 0.29' as='int((nf+2)/2) * W/nf * 0.29'
+ pd='2*int((nf+1)/2) * (W/nf + 0.29)' ps='2*int((nf+2)/2) * (W/nf + 0.29)' nrd='0.29 / W' nrs='0.29 / W'
+ sa=0 sb=0 sd=0 mult=1 m=1
XMDUM4[1] vss vss vss vss sky130_fd_pr__nfet_01v8_lvt L=4 W=1 nf=1 ad='int((nf+1)/2) * W/nf * 0.29' as='int((nf+2)/2) * W/nf * 0.29'
+ pd='2*int((nf+1)/2) * (W/nf + 0.29)' ps='2*int((nf+2)/2) * (W/nf + 0.29)' nrd='0.29 / W' nrs='0.29 / W'
+ sa=0 sb=0 sd=0 mult=1 m=1
XMDUM4[0] vss vss vss vss sky130_fd_pr__nfet_01v8_lvt L=4 W=1 nf=1 ad='int((nf+1)/2) * W/nf * 0.29' as='int((nf+2)/2) * W/nf * 0.29'
+ pd='2*int((nf+1)/2) * (W/nf + 0.29)' ps='2*int((nf+2)/2) * (W/nf + 0.29)' nrd='0.29 / W' nrs='0.29 / W'
+ sa=0 sb=0 sd=0 mult=1 m=1
XMDUM5[3] vbn2 vbn2 vbn2 vss sky130_fd_pr__nfet_01v8_lvt L=4 W=1 nf=1 ad='int((nf+1)/2) * W/nf * 0.29'
+ as='int((nf+2)/2) * W/nf * 0.29' pd='2*int((nf+1)/2) * (W/nf + 0.29)' ps='2*int((nf+2)/2) * (W/nf + 0.29)'
+ nrd='0.29 / W' nrs='0.29 / W' sa=0 sb=0 sd=0 mult=1 m=1
XMDUM5[2] vbn2 vbn2 vbn2 vss sky130_fd_pr__nfet_01v8_lvt L=4 W=1 nf=1 ad='int((nf+1)/2) * W/nf * 0.29'
+ as='int((nf+2)/2) * W/nf * 0.29' pd='2*int((nf+1)/2) * (W/nf + 0.29)' ps='2*int((nf+2)/2) * (W/nf + 0.29)'
+ nrd='0.29 / W' nrs='0.29 / W' sa=0 sb=0 sd=0 mult=1 m=1
XMDUM5[1] vbn2 vbn2 vbn2 vss sky130_fd_pr__nfet_01v8_lvt L=4 W=1 nf=1 ad='int((nf+1)/2) * W/nf * 0.29'
+ as='int((nf+2)/2) * W/nf * 0.29' pd='2*int((nf+1)/2) * (W/nf + 0.29)' ps='2*int((nf+2)/2) * (W/nf + 0.29)'
+ nrd='0.29 / W' nrs='0.29 / W' sa=0 sb=0 sd=0 mult=1 m=1
XMDUM5[0] vbn2 vbn2 vbn2 vss sky130_fd_pr__nfet_01v8_lvt L=4 W=1 nf=1 ad='int((nf+1)/2) * W/nf * 0.29'
+ as='int((nf+2)/2) * W/nf * 0.29' pd='2*int((nf+1)/2) * (W/nf + 0.29)' ps='2*int((nf+2)/2) * (W/nf + 0.29)'
+ nrd='0.29 / W' nrs='0.29 / W' sa=0 sb=0 sd=0 mult=1 m=1
XMDUM6[43] vss vss vss vss sky130_fd_pr__nfet_01v8_lvt L=1 W=1 nf=1 ad='int((nf+1)/2) * W/nf * 0.29'
+ as='int((nf+2)/2) * W/nf * 0.29' pd='2*int((nf+1)/2) * (W/nf + 0.29)' ps='2*int((nf+2)/2) * (W/nf + 0.29)'
+ nrd='0.29 / W' nrs='0.29 / W' sa=0 sb=0 sd=0 mult=1 m=1
XMDUM6[42] vss vss vss vss sky130_fd_pr__nfet_01v8_lvt L=1 W=1 nf=1 ad='int((nf+1)/2) * W/nf * 0.29'
+ as='int((nf+2)/2) * W/nf * 0.29' pd='2*int((nf+1)/2) * (W/nf + 0.29)' ps='2*int((nf+2)/2) * (W/nf + 0.29)'
+ nrd='0.29 / W' nrs='0.29 / W' sa=0 sb=0 sd=0 mult=1 m=1
XMDUM6[41] vss vss vss vss sky130_fd_pr__nfet_01v8_lvt L=1 W=1 nf=1 ad='int((nf+1)/2) * W/nf * 0.29'
+ as='int((nf+2)/2) * W/nf * 0.29' pd='2*int((nf+1)/2) * (W/nf + 0.29)' ps='2*int((nf+2)/2) * (W/nf + 0.29)'
+ nrd='0.29 / W' nrs='0.29 / W' sa=0 sb=0 sd=0 mult=1 m=1
XMDUM6[40] vss vss vss vss sky130_fd_pr__nfet_01v8_lvt L=1 W=1 nf=1 ad='int((nf+1)/2) * W/nf * 0.29'
+ as='int((nf+2)/2) * W/nf * 0.29' pd='2*int((nf+1)/2) * (W/nf + 0.29)' ps='2*int((nf+2)/2) * (W/nf + 0.29)'
+ nrd='0.29 / W' nrs='0.29 / W' sa=0 sb=0 sd=0 mult=1 m=1
XMDUM6[39] vss vss vss vss sky130_fd_pr__nfet_01v8_lvt L=1 W=1 nf=1 ad='int((nf+1)/2) * W/nf * 0.29'
+ as='int((nf+2)/2) * W/nf * 0.29' pd='2*int((nf+1)/2) * (W/nf + 0.29)' ps='2*int((nf+2)/2) * (W/nf + 0.29)'
+ nrd='0.29 / W' nrs='0.29 / W' sa=0 sb=0 sd=0 mult=1 m=1
XMDUM6[38] vss vss vss vss sky130_fd_pr__nfet_01v8_lvt L=1 W=1 nf=1 ad='int((nf+1)/2) * W/nf * 0.29'
+ as='int((nf+2)/2) * W/nf * 0.29' pd='2*int((nf+1)/2) * (W/nf + 0.29)' ps='2*int((nf+2)/2) * (W/nf + 0.29)'
+ nrd='0.29 / W' nrs='0.29 / W' sa=0 sb=0 sd=0 mult=1 m=1
XMDUM6[37] vss vss vss vss sky130_fd_pr__nfet_01v8_lvt L=1 W=1 nf=1 ad='int((nf+1)/2) * W/nf * 0.29'
+ as='int((nf+2)/2) * W/nf * 0.29' pd='2*int((nf+1)/2) * (W/nf + 0.29)' ps='2*int((nf+2)/2) * (W/nf + 0.29)'
+ nrd='0.29 / W' nrs='0.29 / W' sa=0 sb=0 sd=0 mult=1 m=1
XMDUM6[36] vss vss vss vss sky130_fd_pr__nfet_01v8_lvt L=1 W=1 nf=1 ad='int((nf+1)/2) * W/nf * 0.29'
+ as='int((nf+2)/2) * W/nf * 0.29' pd='2*int((nf+1)/2) * (W/nf + 0.29)' ps='2*int((nf+2)/2) * (W/nf + 0.29)'
+ nrd='0.29 / W' nrs='0.29 / W' sa=0 sb=0 sd=0 mult=1 m=1
XMDUM6[35] vss vss vss vss sky130_fd_pr__nfet_01v8_lvt L=1 W=1 nf=1 ad='int((nf+1)/2) * W/nf * 0.29'
+ as='int((nf+2)/2) * W/nf * 0.29' pd='2*int((nf+1)/2) * (W/nf + 0.29)' ps='2*int((nf+2)/2) * (W/nf + 0.29)'
+ nrd='0.29 / W' nrs='0.29 / W' sa=0 sb=0 sd=0 mult=1 m=1
XMDUM6[34] vss vss vss vss sky130_fd_pr__nfet_01v8_lvt L=1 W=1 nf=1 ad='int((nf+1)/2) * W/nf * 0.29'
+ as='int((nf+2)/2) * W/nf * 0.29' pd='2*int((nf+1)/2) * (W/nf + 0.29)' ps='2*int((nf+2)/2) * (W/nf + 0.29)'
+ nrd='0.29 / W' nrs='0.29 / W' sa=0 sb=0 sd=0 mult=1 m=1
XMDUM6[33] vss vss vss vss sky130_fd_pr__nfet_01v8_lvt L=1 W=1 nf=1 ad='int((nf+1)/2) * W/nf * 0.29'
+ as='int((nf+2)/2) * W/nf * 0.29' pd='2*int((nf+1)/2) * (W/nf + 0.29)' ps='2*int((nf+2)/2) * (W/nf + 0.29)'
+ nrd='0.29 / W' nrs='0.29 / W' sa=0 sb=0 sd=0 mult=1 m=1
XMDUM6[32] vss vss vss vss sky130_fd_pr__nfet_01v8_lvt L=1 W=1 nf=1 ad='int((nf+1)/2) * W/nf * 0.29'
+ as='int((nf+2)/2) * W/nf * 0.29' pd='2*int((nf+1)/2) * (W/nf + 0.29)' ps='2*int((nf+2)/2) * (W/nf + 0.29)'
+ nrd='0.29 / W' nrs='0.29 / W' sa=0 sb=0 sd=0 mult=1 m=1
XMDUM6[31] vss vss vss vss sky130_fd_pr__nfet_01v8_lvt L=1 W=1 nf=1 ad='int((nf+1)/2) * W/nf * 0.29'
+ as='int((nf+2)/2) * W/nf * 0.29' pd='2*int((nf+1)/2) * (W/nf + 0.29)' ps='2*int((nf+2)/2) * (W/nf + 0.29)'
+ nrd='0.29 / W' nrs='0.29 / W' sa=0 sb=0 sd=0 mult=1 m=1
XMDUM6[30] vss vss vss vss sky130_fd_pr__nfet_01v8_lvt L=1 W=1 nf=1 ad='int((nf+1)/2) * W/nf * 0.29'
+ as='int((nf+2)/2) * W/nf * 0.29' pd='2*int((nf+1)/2) * (W/nf + 0.29)' ps='2*int((nf+2)/2) * (W/nf + 0.29)'
+ nrd='0.29 / W' nrs='0.29 / W' sa=0 sb=0 sd=0 mult=1 m=1
XMDUM6[29] vss vss vss vss sky130_fd_pr__nfet_01v8_lvt L=1 W=1 nf=1 ad='int((nf+1)/2) * W/nf * 0.29'
+ as='int((nf+2)/2) * W/nf * 0.29' pd='2*int((nf+1)/2) * (W/nf + 0.29)' ps='2*int((nf+2)/2) * (W/nf + 0.29)'
+ nrd='0.29 / W' nrs='0.29 / W' sa=0 sb=0 sd=0 mult=1 m=1
XMDUM6[28] vss vss vss vss sky130_fd_pr__nfet_01v8_lvt L=1 W=1 nf=1 ad='int((nf+1)/2) * W/nf * 0.29'
+ as='int((nf+2)/2) * W/nf * 0.29' pd='2*int((nf+1)/2) * (W/nf + 0.29)' ps='2*int((nf+2)/2) * (W/nf + 0.29)'
+ nrd='0.29 / W' nrs='0.29 / W' sa=0 sb=0 sd=0 mult=1 m=1
XMDUM6[27] vss vss vss vss sky130_fd_pr__nfet_01v8_lvt L=1 W=1 nf=1 ad='int((nf+1)/2) * W/nf * 0.29'
+ as='int((nf+2)/2) * W/nf * 0.29' pd='2*int((nf+1)/2) * (W/nf + 0.29)' ps='2*int((nf+2)/2) * (W/nf + 0.29)'
+ nrd='0.29 / W' nrs='0.29 / W' sa=0 sb=0 sd=0 mult=1 m=1
XMDUM6[26] vss vss vss vss sky130_fd_pr__nfet_01v8_lvt L=1 W=1 nf=1 ad='int((nf+1)/2) * W/nf * 0.29'
+ as='int((nf+2)/2) * W/nf * 0.29' pd='2*int((nf+1)/2) * (W/nf + 0.29)' ps='2*int((nf+2)/2) * (W/nf + 0.29)'
+ nrd='0.29 / W' nrs='0.29 / W' sa=0 sb=0 sd=0 mult=1 m=1
XMDUM6[25] vss vss vss vss sky130_fd_pr__nfet_01v8_lvt L=1 W=1 nf=1 ad='int((nf+1)/2) * W/nf * 0.29'
+ as='int((nf+2)/2) * W/nf * 0.29' pd='2*int((nf+1)/2) * (W/nf + 0.29)' ps='2*int((nf+2)/2) * (W/nf + 0.29)'
+ nrd='0.29 / W' nrs='0.29 / W' sa=0 sb=0 sd=0 mult=1 m=1
XMDUM6[24] vss vss vss vss sky130_fd_pr__nfet_01v8_lvt L=1 W=1 nf=1 ad='int((nf+1)/2) * W/nf * 0.29'
+ as='int((nf+2)/2) * W/nf * 0.29' pd='2*int((nf+1)/2) * (W/nf + 0.29)' ps='2*int((nf+2)/2) * (W/nf + 0.29)'
+ nrd='0.29 / W' nrs='0.29 / W' sa=0 sb=0 sd=0 mult=1 m=1
XMDUM6[23] vss vss vss vss sky130_fd_pr__nfet_01v8_lvt L=1 W=1 nf=1 ad='int((nf+1)/2) * W/nf * 0.29'
+ as='int((nf+2)/2) * W/nf * 0.29' pd='2*int((nf+1)/2) * (W/nf + 0.29)' ps='2*int((nf+2)/2) * (W/nf + 0.29)'
+ nrd='0.29 / W' nrs='0.29 / W' sa=0 sb=0 sd=0 mult=1 m=1
XMDUM6[22] vss vss vss vss sky130_fd_pr__nfet_01v8_lvt L=1 W=1 nf=1 ad='int((nf+1)/2) * W/nf * 0.29'
+ as='int((nf+2)/2) * W/nf * 0.29' pd='2*int((nf+1)/2) * (W/nf + 0.29)' ps='2*int((nf+2)/2) * (W/nf + 0.29)'
+ nrd='0.29 / W' nrs='0.29 / W' sa=0 sb=0 sd=0 mult=1 m=1
XMDUM6[21] vss vss vss vss sky130_fd_pr__nfet_01v8_lvt L=1 W=1 nf=1 ad='int((nf+1)/2) * W/nf * 0.29'
+ as='int((nf+2)/2) * W/nf * 0.29' pd='2*int((nf+1)/2) * (W/nf + 0.29)' ps='2*int((nf+2)/2) * (W/nf + 0.29)'
+ nrd='0.29 / W' nrs='0.29 / W' sa=0 sb=0 sd=0 mult=1 m=1
XMDUM6[20] vss vss vss vss sky130_fd_pr__nfet_01v8_lvt L=1 W=1 nf=1 ad='int((nf+1)/2) * W/nf * 0.29'
+ as='int((nf+2)/2) * W/nf * 0.29' pd='2*int((nf+1)/2) * (W/nf + 0.29)' ps='2*int((nf+2)/2) * (W/nf + 0.29)'
+ nrd='0.29 / W' nrs='0.29 / W' sa=0 sb=0 sd=0 mult=1 m=1
XMDUM6[19] vss vss vss vss sky130_fd_pr__nfet_01v8_lvt L=1 W=1 nf=1 ad='int((nf+1)/2) * W/nf * 0.29'
+ as='int((nf+2)/2) * W/nf * 0.29' pd='2*int((nf+1)/2) * (W/nf + 0.29)' ps='2*int((nf+2)/2) * (W/nf + 0.29)'
+ nrd='0.29 / W' nrs='0.29 / W' sa=0 sb=0 sd=0 mult=1 m=1
XMDUM6[18] vss vss vss vss sky130_fd_pr__nfet_01v8_lvt L=1 W=1 nf=1 ad='int((nf+1)/2) * W/nf * 0.29'
+ as='int((nf+2)/2) * W/nf * 0.29' pd='2*int((nf+1)/2) * (W/nf + 0.29)' ps='2*int((nf+2)/2) * (W/nf + 0.29)'
+ nrd='0.29 / W' nrs='0.29 / W' sa=0 sb=0 sd=0 mult=1 m=1
XMDUM6[17] vss vss vss vss sky130_fd_pr__nfet_01v8_lvt L=1 W=1 nf=1 ad='int((nf+1)/2) * W/nf * 0.29'
+ as='int((nf+2)/2) * W/nf * 0.29' pd='2*int((nf+1)/2) * (W/nf + 0.29)' ps='2*int((nf+2)/2) * (W/nf + 0.29)'
+ nrd='0.29 / W' nrs='0.29 / W' sa=0 sb=0 sd=0 mult=1 m=1
XMDUM6[16] vss vss vss vss sky130_fd_pr__nfet_01v8_lvt L=1 W=1 nf=1 ad='int((nf+1)/2) * W/nf * 0.29'
+ as='int((nf+2)/2) * W/nf * 0.29' pd='2*int((nf+1)/2) * (W/nf + 0.29)' ps='2*int((nf+2)/2) * (W/nf + 0.29)'
+ nrd='0.29 / W' nrs='0.29 / W' sa=0 sb=0 sd=0 mult=1 m=1
XMDUM6[15] vss vss vss vss sky130_fd_pr__nfet_01v8_lvt L=1 W=1 nf=1 ad='int((nf+1)/2) * W/nf * 0.29'
+ as='int((nf+2)/2) * W/nf * 0.29' pd='2*int((nf+1)/2) * (W/nf + 0.29)' ps='2*int((nf+2)/2) * (W/nf + 0.29)'
+ nrd='0.29 / W' nrs='0.29 / W' sa=0 sb=0 sd=0 mult=1 m=1
XMDUM6[14] vss vss vss vss sky130_fd_pr__nfet_01v8_lvt L=1 W=1 nf=1 ad='int((nf+1)/2) * W/nf * 0.29'
+ as='int((nf+2)/2) * W/nf * 0.29' pd='2*int((nf+1)/2) * (W/nf + 0.29)' ps='2*int((nf+2)/2) * (W/nf + 0.29)'
+ nrd='0.29 / W' nrs='0.29 / W' sa=0 sb=0 sd=0 mult=1 m=1
XMDUM6[13] vss vss vss vss sky130_fd_pr__nfet_01v8_lvt L=1 W=1 nf=1 ad='int((nf+1)/2) * W/nf * 0.29'
+ as='int((nf+2)/2) * W/nf * 0.29' pd='2*int((nf+1)/2) * (W/nf + 0.29)' ps='2*int((nf+2)/2) * (W/nf + 0.29)'
+ nrd='0.29 / W' nrs='0.29 / W' sa=0 sb=0 sd=0 mult=1 m=1
XMDUM6[12] vss vss vss vss sky130_fd_pr__nfet_01v8_lvt L=1 W=1 nf=1 ad='int((nf+1)/2) * W/nf * 0.29'
+ as='int((nf+2)/2) * W/nf * 0.29' pd='2*int((nf+1)/2) * (W/nf + 0.29)' ps='2*int((nf+2)/2) * (W/nf + 0.29)'
+ nrd='0.29 / W' nrs='0.29 / W' sa=0 sb=0 sd=0 mult=1 m=1
XMDUM6[11] vss vss vss vss sky130_fd_pr__nfet_01v8_lvt L=1 W=1 nf=1 ad='int((nf+1)/2) * W/nf * 0.29'
+ as='int((nf+2)/2) * W/nf * 0.29' pd='2*int((nf+1)/2) * (W/nf + 0.29)' ps='2*int((nf+2)/2) * (W/nf + 0.29)'
+ nrd='0.29 / W' nrs='0.29 / W' sa=0 sb=0 sd=0 mult=1 m=1
XMDUM6[10] vss vss vss vss sky130_fd_pr__nfet_01v8_lvt L=1 W=1 nf=1 ad='int((nf+1)/2) * W/nf * 0.29'
+ as='int((nf+2)/2) * W/nf * 0.29' pd='2*int((nf+1)/2) * (W/nf + 0.29)' ps='2*int((nf+2)/2) * (W/nf + 0.29)'
+ nrd='0.29 / W' nrs='0.29 / W' sa=0 sb=0 sd=0 mult=1 m=1
XMDUM6[9] vss vss vss vss sky130_fd_pr__nfet_01v8_lvt L=1 W=1 nf=1 ad='int((nf+1)/2) * W/nf * 0.29' as='int((nf+2)/2) * W/nf * 0.29'
+ pd='2*int((nf+1)/2) * (W/nf + 0.29)' ps='2*int((nf+2)/2) * (W/nf + 0.29)' nrd='0.29 / W' nrs='0.29 / W'
+ sa=0 sb=0 sd=0 mult=1 m=1
XMDUM6[8] vss vss vss vss sky130_fd_pr__nfet_01v8_lvt L=1 W=1 nf=1 ad='int((nf+1)/2) * W/nf * 0.29' as='int((nf+2)/2) * W/nf * 0.29'
+ pd='2*int((nf+1)/2) * (W/nf + 0.29)' ps='2*int((nf+2)/2) * (W/nf + 0.29)' nrd='0.29 / W' nrs='0.29 / W'
+ sa=0 sb=0 sd=0 mult=1 m=1
XMDUM6[7] vss vss vss vss sky130_fd_pr__nfet_01v8_lvt L=1 W=1 nf=1 ad='int((nf+1)/2) * W/nf * 0.29' as='int((nf+2)/2) * W/nf * 0.29'
+ pd='2*int((nf+1)/2) * (W/nf + 0.29)' ps='2*int((nf+2)/2) * (W/nf + 0.29)' nrd='0.29 / W' nrs='0.29 / W'
+ sa=0 sb=0 sd=0 mult=1 m=1
XMDUM6[6] vss vss vss vss sky130_fd_pr__nfet_01v8_lvt L=1 W=1 nf=1 ad='int((nf+1)/2) * W/nf * 0.29' as='int((nf+2)/2) * W/nf * 0.29'
+ pd='2*int((nf+1)/2) * (W/nf + 0.29)' ps='2*int((nf+2)/2) * (W/nf + 0.29)' nrd='0.29 / W' nrs='0.29 / W'
+ sa=0 sb=0 sd=0 mult=1 m=1
XMDUM6[5] vss vss vss vss sky130_fd_pr__nfet_01v8_lvt L=1 W=1 nf=1 ad='int((nf+1)/2) * W/nf * 0.29' as='int((nf+2)/2) * W/nf * 0.29'
+ pd='2*int((nf+1)/2) * (W/nf + 0.29)' ps='2*int((nf+2)/2) * (W/nf + 0.29)' nrd='0.29 / W' nrs='0.29 / W'
+ sa=0 sb=0 sd=0 mult=1 m=1
XMDUM6[4] vss vss vss vss sky130_fd_pr__nfet_01v8_lvt L=1 W=1 nf=1 ad='int((nf+1)/2) * W/nf * 0.29' as='int((nf+2)/2) * W/nf * 0.29'
+ pd='2*int((nf+1)/2) * (W/nf + 0.29)' ps='2*int((nf+2)/2) * (W/nf + 0.29)' nrd='0.29 / W' nrs='0.29 / W'
+ sa=0 sb=0 sd=0 mult=1 m=1
XMDUM6[3] vss vss vss vss sky130_fd_pr__nfet_01v8_lvt L=1 W=1 nf=1 ad='int((nf+1)/2) * W/nf * 0.29' as='int((nf+2)/2) * W/nf * 0.29'
+ pd='2*int((nf+1)/2) * (W/nf + 0.29)' ps='2*int((nf+2)/2) * (W/nf + 0.29)' nrd='0.29 / W' nrs='0.29 / W'
+ sa=0 sb=0 sd=0 mult=1 m=1
XMDUM6[2] vss vss vss vss sky130_fd_pr__nfet_01v8_lvt L=1 W=1 nf=1 ad='int((nf+1)/2) * W/nf * 0.29' as='int((nf+2)/2) * W/nf * 0.29'
+ pd='2*int((nf+1)/2) * (W/nf + 0.29)' ps='2*int((nf+2)/2) * (W/nf + 0.29)' nrd='0.29 / W' nrs='0.29 / W'
+ sa=0 sb=0 sd=0 mult=1 m=1
XMDUM6[1] vss vss vss vss sky130_fd_pr__nfet_01v8_lvt L=1 W=1 nf=1 ad='int((nf+1)/2) * W/nf * 0.29' as='int((nf+2)/2) * W/nf * 0.29'
+ pd='2*int((nf+1)/2) * (W/nf + 0.29)' ps='2*int((nf+2)/2) * (W/nf + 0.29)' nrd='0.29 / W' nrs='0.29 / W'
+ sa=0 sb=0 sd=0 mult=1 m=1
XMDUM6[0] vss vss vss vss sky130_fd_pr__nfet_01v8_lvt L=1 W=1 nf=1 ad='int((nf+1)/2) * W/nf * 0.29' as='int((nf+2)/2) * W/nf * 0.29'
+ pd='2*int((nf+1)/2) * (W/nf + 0.29)' ps='2*int((nf+2)/2) * (W/nf + 0.29)' nrd='0.29 / W' nrs='0.29 / W'
+ sa=0 sb=0 sd=0 mult=1 m=1
XMDUM7[3] diff diff diff vdd sky130_fd_pr__pfet_01v8_lvt L=1 W=4 nf=1 ad='int((nf+1)/2) * W/nf * 0.29'
+ as='int((nf+2)/2) * W/nf * 0.29' pd='2*int((nf+1)/2) * (W/nf + 0.29)' ps='2*int((nf+2)/2) * (W/nf + 0.29)'
+ nrd='0.29 / W' nrs='0.29 / W' sa=0 sb=0 sd=0 mult=1 m=1
XMDUM7[2] diff diff diff vdd sky130_fd_pr__pfet_01v8_lvt L=1 W=4 nf=1 ad='int((nf+1)/2) * W/nf * 0.29'
+ as='int((nf+2)/2) * W/nf * 0.29' pd='2*int((nf+1)/2) * (W/nf + 0.29)' ps='2*int((nf+2)/2) * (W/nf + 0.29)'
+ nrd='0.29 / W' nrs='0.29 / W' sa=0 sb=0 sd=0 mult=1 m=1
XMDUM7[1] diff diff diff vdd sky130_fd_pr__pfet_01v8_lvt L=1 W=4 nf=1 ad='int((nf+1)/2) * W/nf * 0.29'
+ as='int((nf+2)/2) * W/nf * 0.29' pd='2*int((nf+1)/2) * (W/nf + 0.29)' ps='2*int((nf+2)/2) * (W/nf + 0.29)'
+ nrd='0.29 / W' nrs='0.29 / W' sa=0 sb=0 sd=0 mult=1 m=1
XMDUM7[0] diff diff diff vdd sky130_fd_pr__pfet_01v8_lvt L=1 W=4 nf=1 ad='int((nf+1)/2) * W/nf * 0.29'
+ as='int((nf+2)/2) * W/nf * 0.29' pd='2*int((nf+1)/2) * (W/nf + 0.29)' ps='2*int((nf+2)/2) * (W/nf + 0.29)'
+ nrd='0.29 / W' nrs='0.29 / W' sa=0 sb=0 sd=0 mult=1 m=1
.ends

.GLOBAL GND
.end
